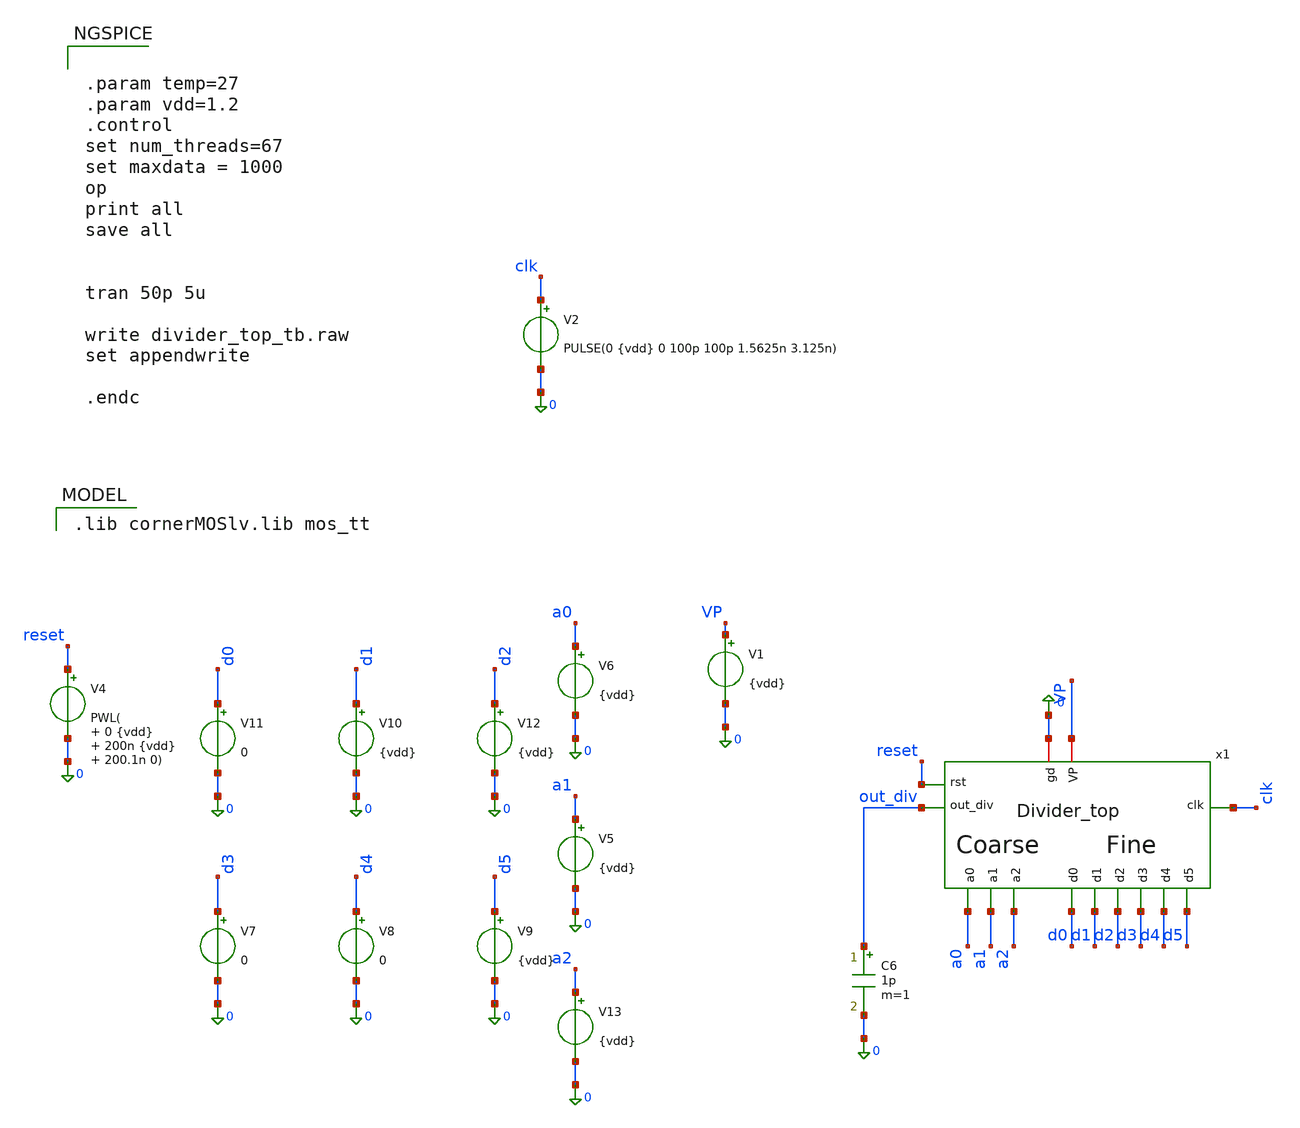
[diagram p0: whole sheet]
** sch_path: schematics/divider/tb/divider_top_tb.sch
**.subckt divider_top_tb
V1 VP 0 {vdd}
V2 clk 0 PULSE(0 {vdd} 0 100p 100p 1.5625n 3.125n)
V8 d4 0 0
V9 d5 0 {vdd}
V11 d0 0 0
V10 d1 0 {vdd}
V12 d2 0 {vdd}
V7 d3 0 0
V5 a1 0 {vdd}
V6 a0 0 {vdd}
V13 a2 0 {vdd}
C6 out_div 0 1p m=1
x1 0 VP clk d0 d1 d2 d3 d4 d5 a0 a1 a2 out_div reset Divider_top
V4 reset 0 PWL( 0 {vdd} 200n {vdd} 200.1n 0)
**** begin user architecture code


.param temp=27
.param vdd=1.2
.control
set num_threads=67
set maxdata = 1000
op
print all
save all


tran 50p 5u

write divider_top_tb.raw
set appendwrite

.endc


 .lib cornerMOSlv.lib mos_tt

**** end user architecture code
**.ends
.end
